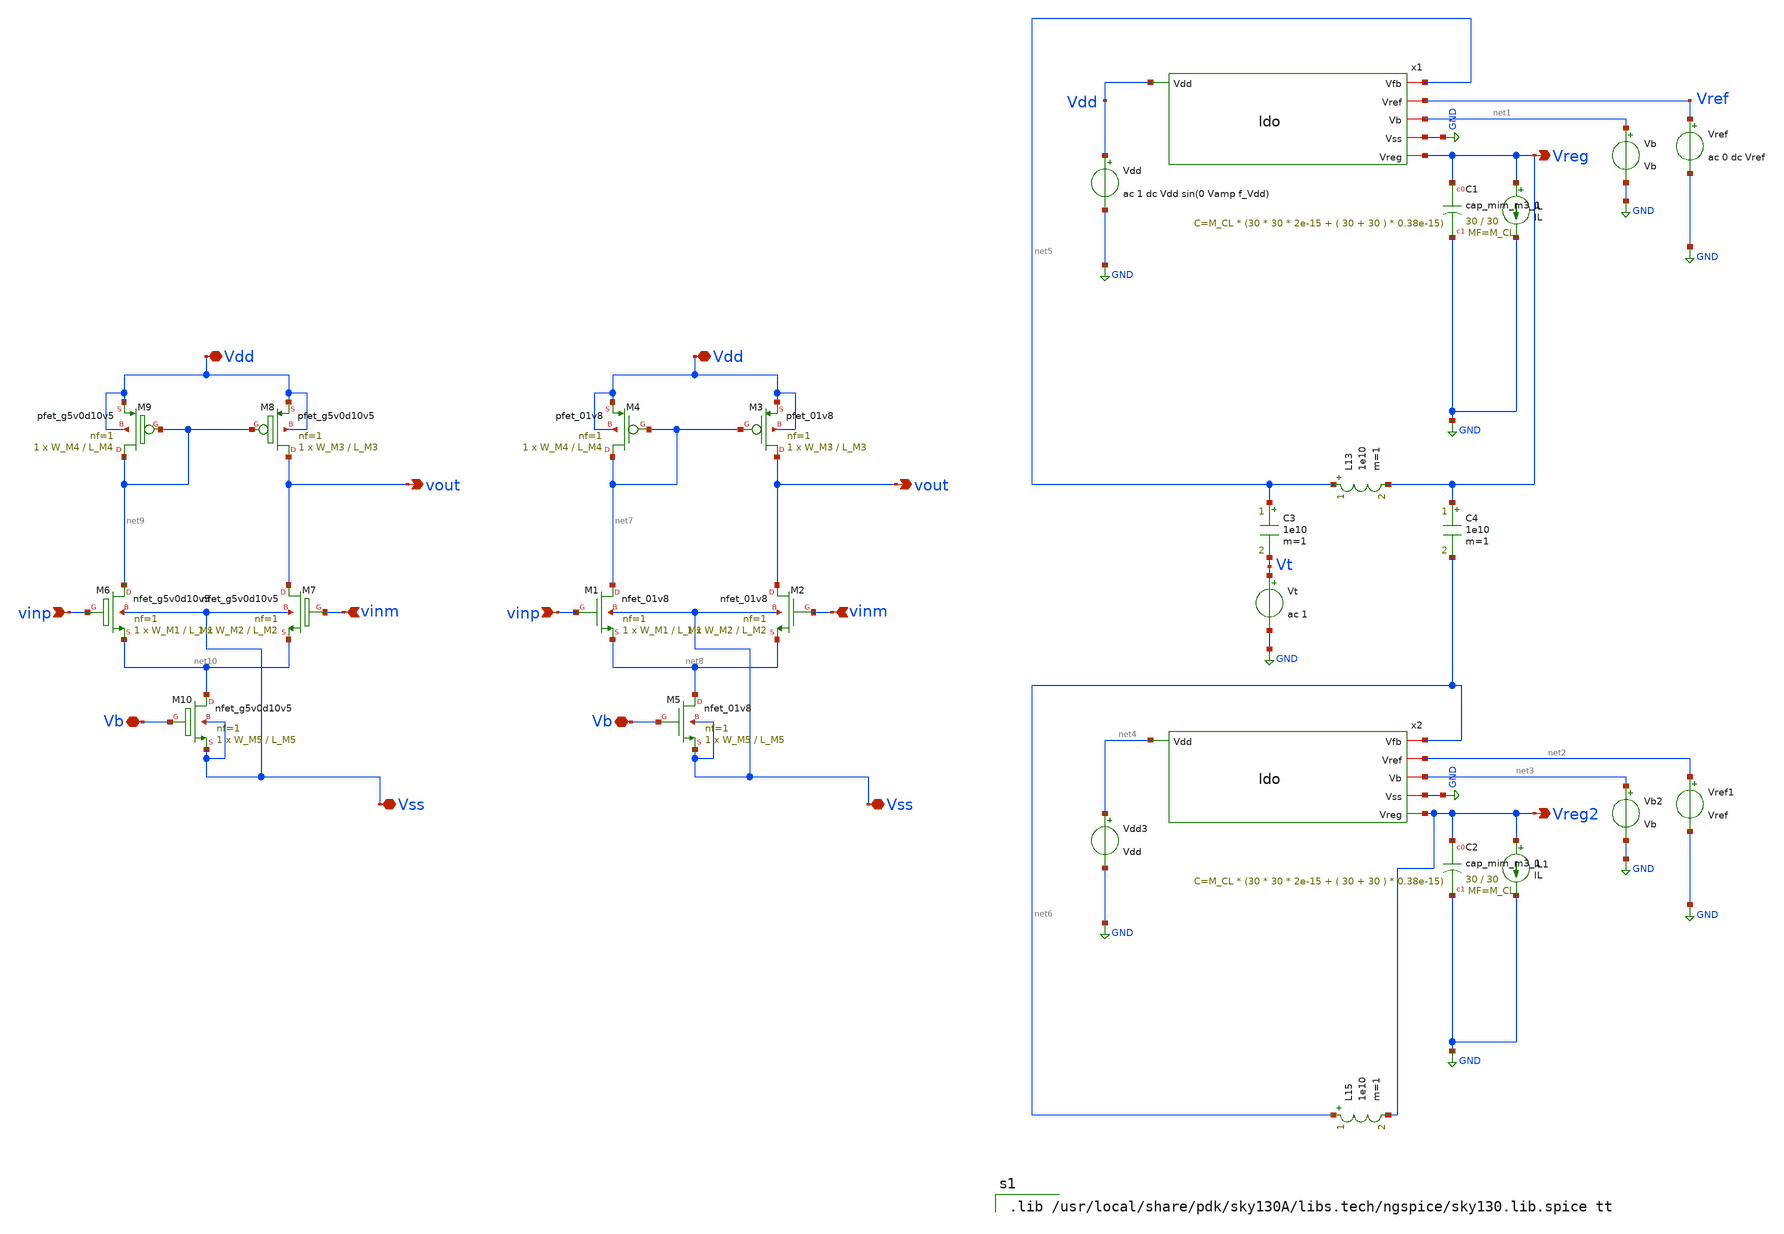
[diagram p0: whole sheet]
** sch_path: xschem/ldo_tb2.sch
**.subckt ldo_tb2 Vreg Vreg2 Vdd vinm vinp Vb vout Vss Vdd vinm vinp Vb vout Vss
*.opin Vreg
*.opin Vreg2
*.iopin Vdd
*.ipin vinm
*.ipin vinp
*.iopin Vb
*.opin vout
*.iopin Vss
*.iopin Vdd
*.ipin vinm
*.ipin vinp
*.iopin Vb
*.opin vout
*.iopin Vss
Vref Vref GND ac 0 dc Vref
Vb net1 GND Vb
IL Vreg GND IL
Vdd Vdd GND ac 1 dc Vdd sin(0 Vamp f_Vdd)
x1 Vdd net5 Vref net1 GND Vreg ldo
Vref1 net2 GND Vref
Vb2 net3 GND Vb
IL1 Vreg2 GND IL
Vdd3 net4 GND Vdd
x2 net4 net6 net2 net3 GND Vreg2 ldo
L13 net5 Vreg 1e10 m=1
C3 net5 Vt 1e10 m=1
Vt Vt GND ac 1
C4 Vreg net6 1e10 m=1
L15 net6 Vreg2 1e10 m=1
XM5 net8 Vb Vss Vss sky130_fd_pr__nfet_01v8 L=L_M5 W=W_M5 nf=1 ad='int((nf+1)/2) * W/nf * 0.29' as='int((nf+2)/2) * W/nf * 0.29'
+ pd='2*int((nf+1)/2) * (W/nf + 0.29)' ps='2*int((nf+2)/2) * (W/nf + 0.29)' nrd='0.29 / W' nrs='0.29 / W'
+ sa=0 sb=0 sd=0 mult=1 m=1
XM3 vout net7 Vdd Vdd sky130_fd_pr__pfet_01v8 L=L_M3 W=W_M3 nf=1 ad='int((nf+1)/2) * W/nf * 0.29' as='int((nf+2)/2) * W/nf * 0.29'
+ pd='2*int((nf+1)/2) * (W/nf + 0.29)' ps='2*int((nf+2)/2) * (W/nf + 0.29)' nrd='0.29 / W' nrs='0.29 / W'
+ sa=0 sb=0 sd=0 mult=1 m=1
XM4 net7 net7 Vdd Vdd sky130_fd_pr__pfet_01v8 L=L_M4 W=W_M4 nf=1 ad='int((nf+1)/2) * W/nf * 0.29' as='int((nf+2)/2) * W/nf * 0.29'
+ pd='2*int((nf+1)/2) * (W/nf + 0.29)' ps='2*int((nf+2)/2) * (W/nf + 0.29)' nrd='0.29 / W' nrs='0.29 / W'
+ sa=0 sb=0 sd=0 mult=1 m=1
XM1 net7 vinp net8 Vss sky130_fd_pr__nfet_01v8 L=L_M1 W=W_M1 nf=1 ad='int((nf+1)/2) * W/nf * 0.29' as='int((nf+2)/2) * W/nf * 0.29'
+ pd='2*int((nf+1)/2) * (W/nf + 0.29)' ps='2*int((nf+2)/2) * (W/nf + 0.29)' nrd='0.29 / W' nrs='0.29 / W'
+ sa=0 sb=0 sd=0 mult=1 m=1
XM2 vout vinm net8 Vss sky130_fd_pr__nfet_01v8 L=L_M2 W=W_M2 nf=1 ad='int((nf+1)/2) * W/nf * 0.29' as='int((nf+2)/2) * W/nf * 0.29'
+ pd='2*int((nf+1)/2) * (W/nf + 0.29)' ps='2*int((nf+2)/2) * (W/nf + 0.29)' nrd='0.29 / W' nrs='0.29 / W'
+ sa=0 sb=0 sd=0 mult=1 m=1
XM6 net9 vinp net10 Vss sky130_fd_pr__nfet_g5v0d10v5 L=L_M1 W=W_M1 nf=1 ad='int((nf+1)/2) * W/nf * 0.29'
+ as='int((nf+2)/2) * W/nf * 0.29' pd='2*int((nf+1)/2) * (W/nf + 0.29)' ps='2*int((nf+2)/2) * (W/nf + 0.29)'
+ nrd='0.29 / W' nrs='0.29 / W' sa=0 sb=0 sd=0 mult=1 m=1
XM7 vout vinm net10 Vss sky130_fd_pr__nfet_g5v0d10v5 L=L_M2 W=W_M2 nf=1 ad='int((nf+1)/2) * W/nf * 0.29'
+ as='int((nf+2)/2) * W/nf * 0.29' pd='2*int((nf+1)/2) * (W/nf + 0.29)' ps='2*int((nf+2)/2) * (W/nf + 0.29)'
+ nrd='0.29 / W' nrs='0.29 / W' sa=0 sb=0 sd=0 mult=1 m=1
XM8 vout net9 Vdd Vdd sky130_fd_pr__pfet_g5v0d10v5 L=L_M3 W=W_M3 nf=1 ad='int((nf+1)/2) * W/nf * 0.29'
+ as='int((nf+2)/2) * W/nf * 0.29' pd='2*int((nf+1)/2) * (W/nf + 0.29)' ps='2*int((nf+2)/2) * (W/nf + 0.29)'
+ nrd='0.29 / W' nrs='0.29 / W' sa=0 sb=0 sd=0 mult=1 m=1
XM9 net9 net9 Vdd Vdd sky130_fd_pr__pfet_g5v0d10v5 L=L_M4 W=W_M4 nf=1 ad='int((nf+1)/2) * W/nf * 0.29'
+ as='int((nf+2)/2) * W/nf * 0.29' pd='2*int((nf+1)/2) * (W/nf + 0.29)' ps='2*int((nf+2)/2) * (W/nf + 0.29)'
+ nrd='0.29 / W' nrs='0.29 / W' sa=0 sb=0 sd=0 mult=1 m=1
XM10 net10 Vb Vss Vss sky130_fd_pr__nfet_g5v0d10v5 L=L_M5 W=W_M5 nf=1 ad='int((nf+1)/2) * W/nf * 0.29'
+ as='int((nf+2)/2) * W/nf * 0.29' pd='2*int((nf+1)/2) * (W/nf + 0.29)' ps='2*int((nf+2)/2) * (W/nf + 0.29)'
+ nrd='0.29 / W' nrs='0.29 / W' sa=0 sb=0 sd=0 mult=1 m=1
XC1 Vreg GND sky130_fd_pr__cap_mim_m3_1 W=30 L=30 MF=M_CL m=M_CL
XC2 Vreg2 GND sky130_fd_pr__cap_mim_m3_1 W=30 L=30 MF=M_CL m=M_CL
**** begin user architecture code

.lib /usr/local/share/pdk/sky130A/libs.tech/ngspice/sky130.lib.spice tt



.control
save all
set filetype=ascii
set units=degrees

* DC sweep
dc Vdd 0 3 0.01
plot v(Vdd) v(Vreg)
wrdata ldo_tb_dc v(Vreg)

* Stability_Analysis ver2 using large ind and cap
alter IL dc=100u
alter Vdd ac=0
alter Vref ac=0
alter Vt ac=1
ac dec 100 1 10G
let L2=-v(Vreg)/v(Vt)
plot vdb(L2) vp(L2) xlog

.endc



.include /autofs/fs1.ece/fs1.eecg.tcc/lizongh2/sky130_ldo/xschem/simulations/ldo_tb_vars.spice


**** end user architecture code
**.ends

* expanding   symbol:  ldo.sym # of pins=6
** sym_path: xschem/ldo.sym
** sch_path: xschem/ldo.sch
.subckt ldo Vdd Vfb Vref Vb Vss Vreg
*.iopin Vb
*.iopin Vss
*.opin Vreg
*.iopin Vref
*.ipin Vdd
*.iopin Vfb
x1 Vdd net1 Vfb Vref Vb Vss diff_pair
XM6 Vreg net1 Vdd Vdd sky130_fd_pr__pfet_g5v0d10v5 L=L_pass W=W_pass nf=Nf_pass ad='int((nf+1)/2) * W/nf * 0.29'
+ as='int((nf+2)/2) * W/nf * 0.29' pd='2*int((nf+1)/2) * (W/nf + 0.29)' ps='2*int((nf+2)/2) * (W/nf + 0.29)'
+ nrd='0.29 / W' nrs='0.29 / W' sa=0 sb=0 sd=0 mult=M_pass m=M_pass
XCfb net2 Vreg sky130_fd_pr__cap_mim_m3_1 W=10 L=10 MF=M_Cfb m=M_Cfb
XRfb net2 net1 Vss sky130_fd_pr__res_high_po_0p35 L=3 mult=M_Rfb m=M_Rfb
.ends


* expanding   symbol:  diff_pair.sym # of pins=6
** sym_path: xschem/diff_pair.sym
** sch_path: xschem/diff_pair.sch
.subckt diff_pair Vdd vout vinp vinm Vb Vss
*.iopin Vdd
*.ipin vinm
*.ipin vinp
*.iopin Vb
*.opin vout
*.iopin Vss
XM1 net1 vinp net2 Vss sky130_fd_pr__nfet_g5v0d10v5 L=L_M1 W=W_M1 nf=1 ad='int((nf+1)/2) * W/nf * 0.29'
+ as='int((nf+2)/2) * W/nf * 0.29' pd='2*int((nf+1)/2) * (W/nf + 0.29)' ps='2*int((nf+2)/2) * (W/nf + 0.29)'
+ nrd='0.29 / W' nrs='0.29 / W' sa=0 sb=0 sd=0 mult=1 m=1
XM2 vout vinm net2 Vss sky130_fd_pr__nfet_g5v0d10v5 L=L_M2 W=W_M2 nf=1 ad='int((nf+1)/2) * W/nf * 0.29'
+ as='int((nf+2)/2) * W/nf * 0.29' pd='2*int((nf+1)/2) * (W/nf + 0.29)' ps='2*int((nf+2)/2) * (W/nf + 0.29)'
+ nrd='0.29 / W' nrs='0.29 / W' sa=0 sb=0 sd=0 mult=1 m=1
XM3 vout net1 Vdd Vdd sky130_fd_pr__pfet_g5v0d10v5 L=L_M3 W=W_M3 nf=1 ad='int((nf+1)/2) * W/nf * 0.29'
+ as='int((nf+2)/2) * W/nf * 0.29' pd='2*int((nf+1)/2) * (W/nf + 0.29)' ps='2*int((nf+2)/2) * (W/nf + 0.29)'
+ nrd='0.29 / W' nrs='0.29 / W' sa=0 sb=0 sd=0 mult=1 m=1
XM4 net1 net1 Vdd Vdd sky130_fd_pr__pfet_g5v0d10v5 L=L_M4 W=W_M4 nf=1 ad='int((nf+1)/2) * W/nf * 0.29'
+ as='int((nf+2)/2) * W/nf * 0.29' pd='2*int((nf+1)/2) * (W/nf + 0.29)' ps='2*int((nf+2)/2) * (W/nf + 0.29)'
+ nrd='0.29 / W' nrs='0.29 / W' sa=0 sb=0 sd=0 mult=1 m=1
XM5 net2 Vb Vss Vss sky130_fd_pr__nfet_g5v0d10v5 L=L_M5 W=W_M5 nf=1 ad='int((nf+1)/2) * W/nf * 0.29'
+ as='int((nf+2)/2) * W/nf * 0.29' pd='2*int((nf+1)/2) * (W/nf + 0.29)' ps='2*int((nf+2)/2) * (W/nf + 0.29)'
+ nrd='0.29 / W' nrs='0.29 / W' sa=0 sb=0 sd=0 mult=1 m=1
.ends

.GLOBAL GND
.end
